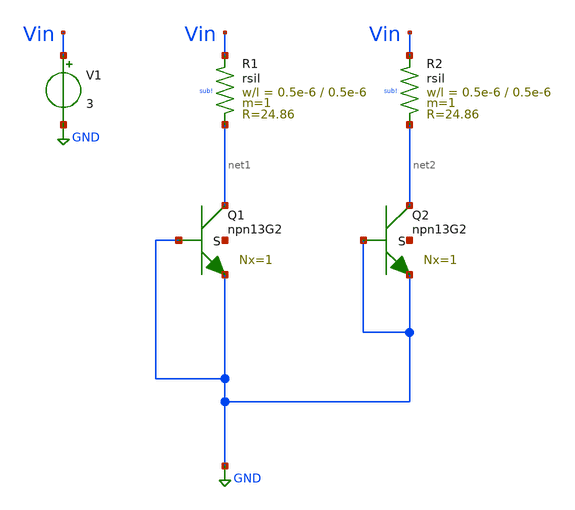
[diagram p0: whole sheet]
** sch_path: xschem/untitled.sch
**.subckt untitled
XQ1 net1 GND GND net3 npn13G2 Nx=1 mm_ok=1
XQ2 net2 GND GND net4 npn13G2 Nx=1 mm_ok=1
XR1 Vin net1 sub! rsil w=0.5e-6 l=0.5e-6 m=1 mm_ok=1
XR2 Vin net2 sub! rsil w=0.5e-6 l=0.5e-6 m=1 mm_ok=1
V1 Vin GND 3
**.ends
.GLOBAL GND
.end
